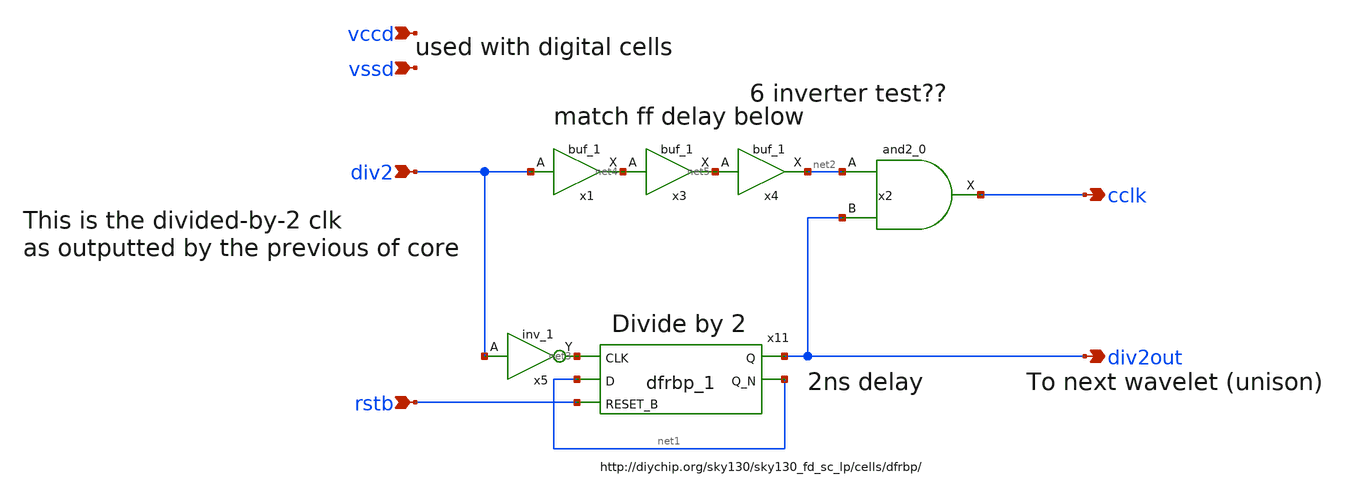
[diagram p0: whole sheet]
** sch_path: xschem/clkgen/dig_div2.sch
**.subckt dig_div2 div2 rstb cclk div2out vccd vssd
*.ipin div2
*.ipin rstb
*.opin cclk
*.opin div2out
*.ipin vccd
*.ipin vssd
x11 net3 net1 rstb vssd vssd vccd vccd div2out net1 sky130_fd_sc_hd__dfrbp_1
x2 net2 div2out vssd vssd vccd vccd cclk sky130_fd_sc_hd__and2_0
x1 div2 vssd vssd vccd vccd net4 sky130_fd_sc_hd__buf_1
x3 net4 vssd vssd vccd vccd net5 sky130_fd_sc_hd__buf_1
x4 net5 vssd vssd vccd vccd net2 sky130_fd_sc_hd__buf_1
x5 div2 vssd vssd vccd vccd net3 sky130_fd_sc_hd__inv_1
**.ends
.end
